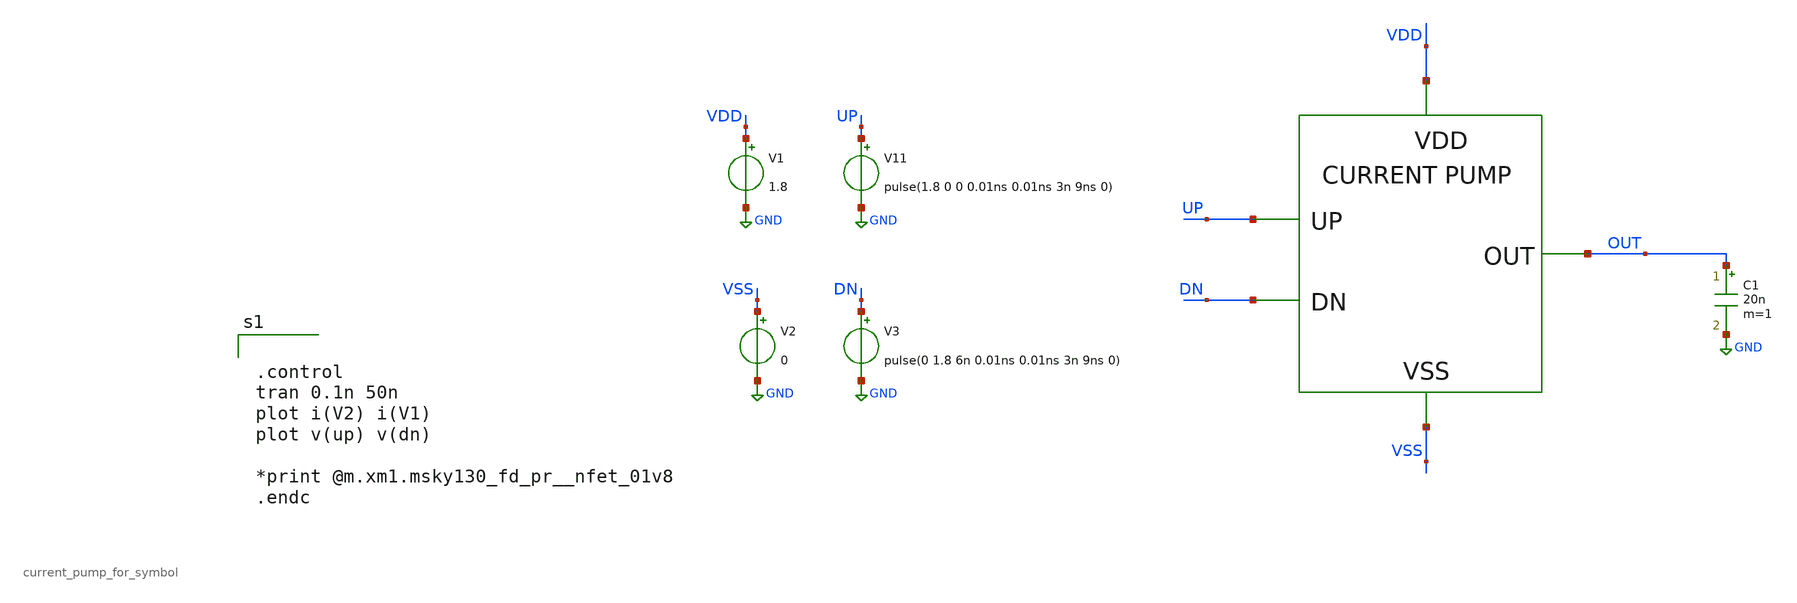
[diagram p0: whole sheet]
** sch_path: xschem/DC_DC_Converter_xschem/DC_DC_Converter/current_pump/current_pump_for_symbol_TB.sch
**.subckt current_pump_for_symbol_TB
X1 UP OUT VDD VSS DN current_pump_for_symbol
C1 OUT GND 20n m=1
V11 UP GND pulse(1.8 0 0 0.01ns 0.01ns 3n 9ns 0)
V3 DN GND pulse(0 1.8 6n 0.01ns 0.01ns 3n 9ns 0)
V1 VDD GND 1.8
V2 VSS GND 0
**** begin user architecture code

** opencircuitdesign pdks install
.lib $::SKYWATER_MODELS/sky130.lib.spice tt




.control
tran 0.1n 50n
plot i(V2) i(V1)
plot v(up) v(dn)

*print @m.xm1.msky130_fd_pr__nfet_01v8
.endc


**** end user architecture code
**.ends

* expanding   symbol:  DC_DC_Converter/current_pump/current_pump_for_symbol.sym # of pins=5
** sym_path: xschem/DC_DC_Converter_xschem/DC_DC_Converter/current_pump/current_pump_for_symbol.sym
** sch_path: xschem/DC_DC_Converter_xschem/DC_DC_Converter/current_pump/current_pump_for_symbol.sch
.subckt current_pump_for_symbol UP VOUT VDD VSS DN
*.iopin VDD
*.iopin UP
*.iopin DN
*.iopin VSS
*.iopin VOUT
XM1 VOUT DN net1 VSS sky130_fd_pr__nfet_01v8 L=0.15 W=20 nf=20 ad='int((nf+1)/2) * W/nf * 0.29' as='int((nf+2)/2) * W/nf * 0.29'
+ pd='2*int((nf+1)/2) * (W/nf + 0.29)' ps='2*int((nf+2)/2) * (W/nf + 0.29)' nrd='0.29 / W' nrs='0.29 / W'
+ sa=0 sb=0 sd=0 mult=1 m=1
XM2 VOUT UP net2 VDD sky130_fd_pr__pfet_01v8 L=0.15 W=60 nf=20 ad='int((nf+1)/2) * W/nf * 0.29' as='int((nf+2)/2) * W/nf * 0.29'
+ pd='2*int((nf+1)/2) * (W/nf + 0.29)' ps='2*int((nf+2)/2) * (W/nf + 0.29)' nrd='0.29 / W' nrs='0.29 / W'
+ sa=0 sb=0 sd=0 mult=1 m=1
R1 net2 VDD sky130_fd_pr__res_generic_m1 W=0.14 L=14.23 m=1
R2 VSS net1 sky130_fd_pr__res_generic_m1 W=0.14 L=11.21 m=1
.ends

.GLOBAL GND
.end
